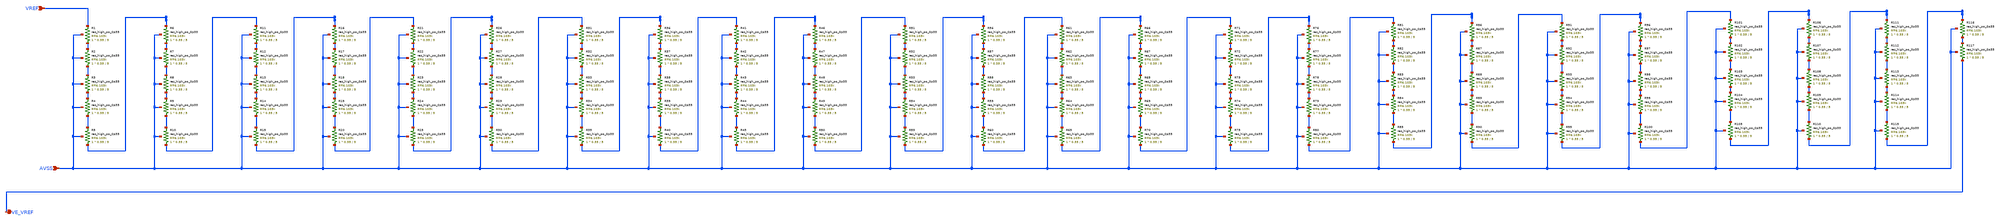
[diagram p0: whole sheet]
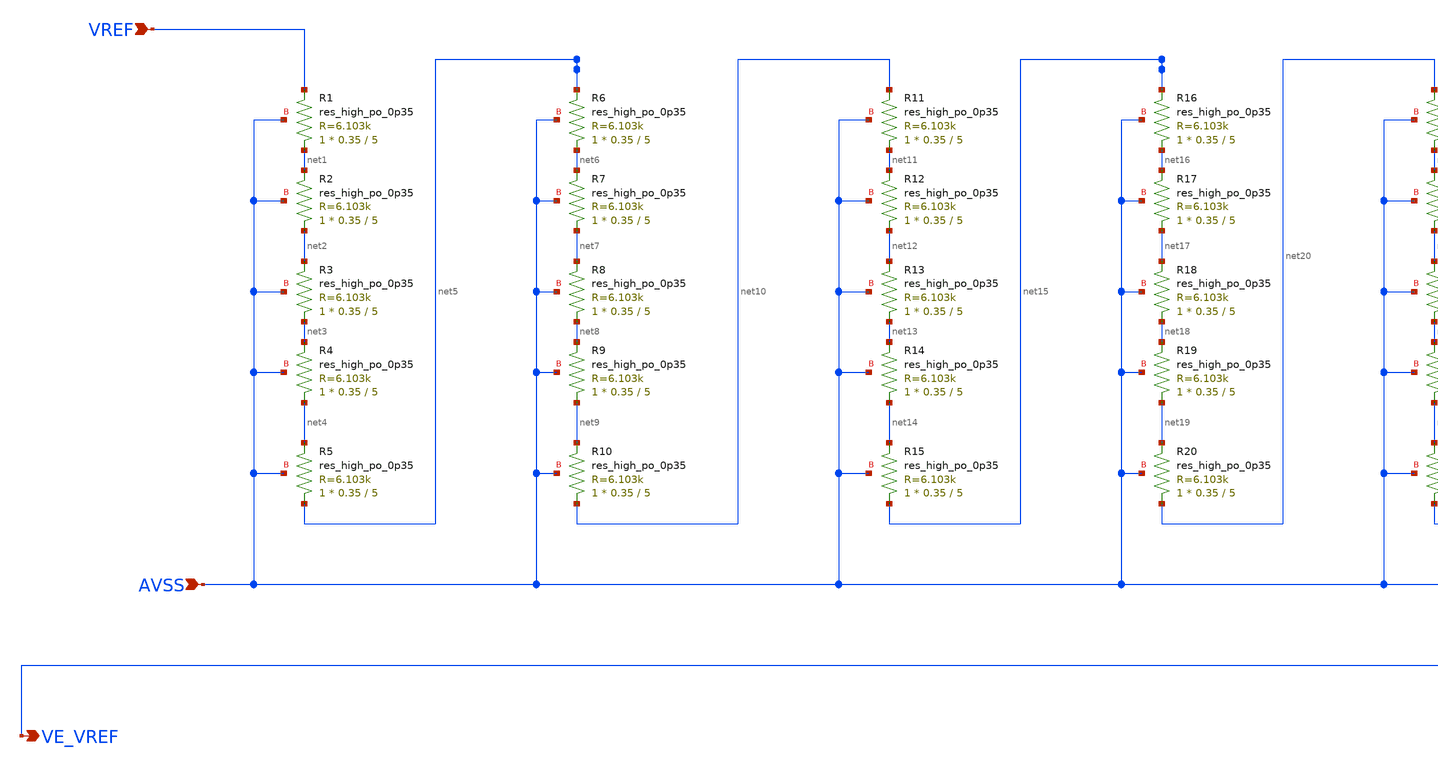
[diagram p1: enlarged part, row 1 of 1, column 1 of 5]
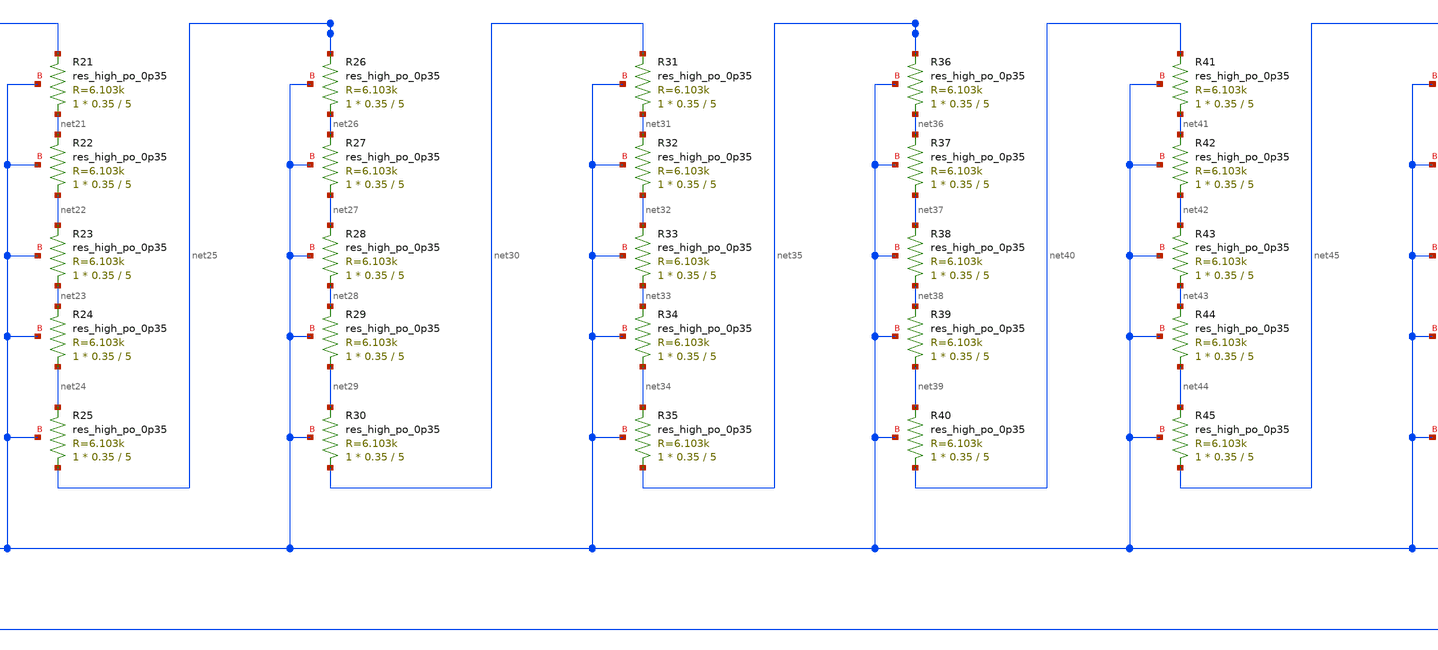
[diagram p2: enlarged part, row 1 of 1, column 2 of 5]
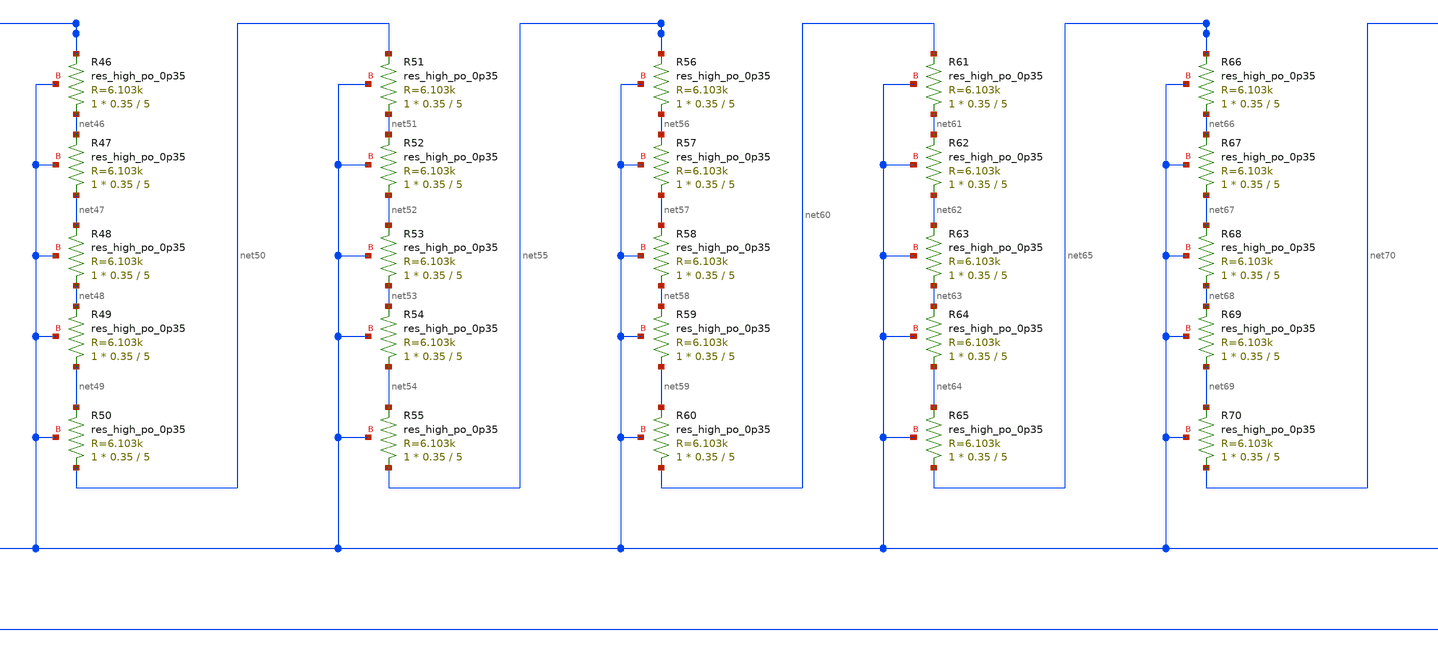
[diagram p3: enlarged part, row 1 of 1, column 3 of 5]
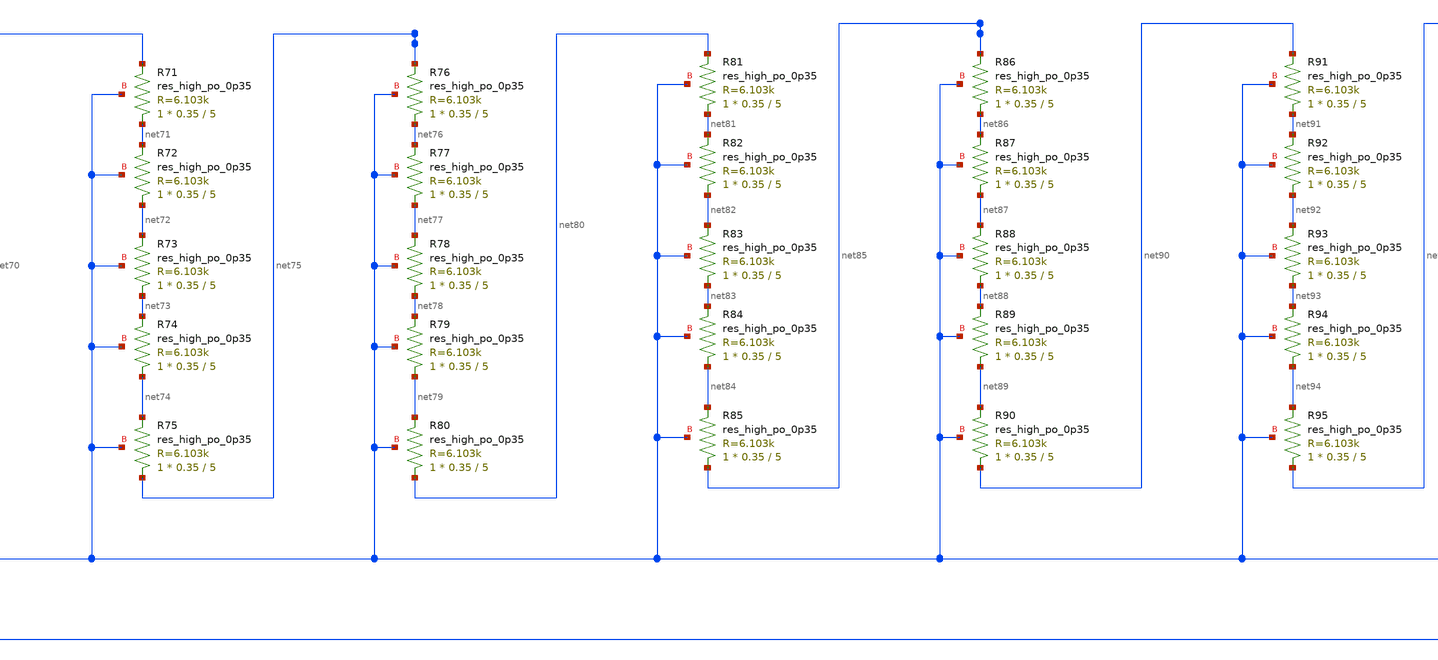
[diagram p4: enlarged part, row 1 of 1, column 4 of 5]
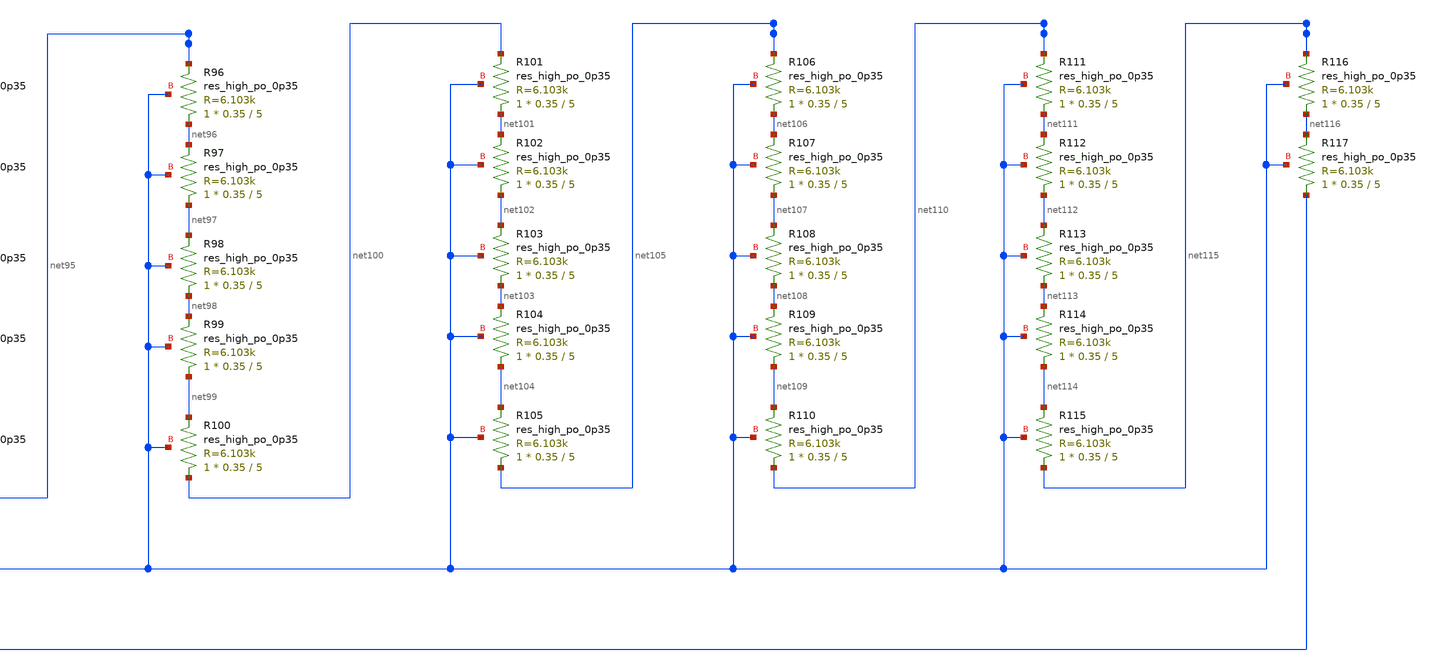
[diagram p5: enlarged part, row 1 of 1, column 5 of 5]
** sch_path: lef/bg2_res_array_vref.sch
**.subckt bg2_res_array_vref VREF VE_VREF AVSS
*.ipin VREF
*.opin VE_VREF
*.ipin AVSS
XR1 net1 VREF AVSS sky130_fd_pr__res_high_po_0p35 L=5 mult=1 m=1
XR2 net2 net1 AVSS sky130_fd_pr__res_high_po_0p35 L=5 mult=1 m=1
XR3 net3 net2 AVSS sky130_fd_pr__res_high_po_0p35 L=5 mult=1 m=1
XR4 net4 net3 AVSS sky130_fd_pr__res_high_po_0p35 L=5 mult=1 m=1
XR5 net5 net4 AVSS sky130_fd_pr__res_high_po_0p35 L=5 mult=1 m=1
XR6 net6 net5 AVSS sky130_fd_pr__res_high_po_0p35 L=5 mult=1 m=1
XR7 net7 net6 AVSS sky130_fd_pr__res_high_po_0p35 L=5 mult=1 m=1
XR8 net8 net7 AVSS sky130_fd_pr__res_high_po_0p35 L=5 mult=1 m=1
XR9 net9 net8 AVSS sky130_fd_pr__res_high_po_0p35 L=5 mult=1 m=1
XR10 net10 net9 AVSS sky130_fd_pr__res_high_po_0p35 L=5 mult=1 m=1
XR11 net11 net10 AVSS sky130_fd_pr__res_high_po_0p35 L=5 mult=1 m=1
XR12 net12 net11 AVSS sky130_fd_pr__res_high_po_0p35 L=5 mult=1 m=1
XR13 net13 net12 AVSS sky130_fd_pr__res_high_po_0p35 L=5 mult=1 m=1
XR14 net14 net13 AVSS sky130_fd_pr__res_high_po_0p35 L=5 mult=1 m=1
XR15 net15 net14 AVSS sky130_fd_pr__res_high_po_0p35 L=5 mult=1 m=1
XR16 net16 net15 AVSS sky130_fd_pr__res_high_po_0p35 L=5 mult=1 m=1
XR17 net17 net16 AVSS sky130_fd_pr__res_high_po_0p35 L=5 mult=1 m=1
XR18 net18 net17 AVSS sky130_fd_pr__res_high_po_0p35 L=5 mult=1 m=1
XR19 net19 net18 AVSS sky130_fd_pr__res_high_po_0p35 L=5 mult=1 m=1
XR20 net20 net19 AVSS sky130_fd_pr__res_high_po_0p35 L=5 mult=1 m=1
XR21 net21 net20 AVSS sky130_fd_pr__res_high_po_0p35 L=5 mult=1 m=1
XR22 net22 net21 AVSS sky130_fd_pr__res_high_po_0p35 L=5 mult=1 m=1
XR23 net23 net22 AVSS sky130_fd_pr__res_high_po_0p35 L=5 mult=1 m=1
XR24 net24 net23 AVSS sky130_fd_pr__res_high_po_0p35 L=5 mult=1 m=1
XR25 net25 net24 AVSS sky130_fd_pr__res_high_po_0p35 L=5 mult=1 m=1
XR26 net26 net25 AVSS sky130_fd_pr__res_high_po_0p35 L=5 mult=1 m=1
XR27 net27 net26 AVSS sky130_fd_pr__res_high_po_0p35 L=5 mult=1 m=1
XR28 net28 net27 AVSS sky130_fd_pr__res_high_po_0p35 L=5 mult=1 m=1
XR29 net29 net28 AVSS sky130_fd_pr__res_high_po_0p35 L=5 mult=1 m=1
XR30 net30 net29 AVSS sky130_fd_pr__res_high_po_0p35 L=5 mult=1 m=1
XR31 net31 net30 AVSS sky130_fd_pr__res_high_po_0p35 L=5 mult=1 m=1
XR32 net32 net31 AVSS sky130_fd_pr__res_high_po_0p35 L=5 mult=1 m=1
XR33 net33 net32 AVSS sky130_fd_pr__res_high_po_0p35 L=5 mult=1 m=1
XR34 net34 net33 AVSS sky130_fd_pr__res_high_po_0p35 L=5 mult=1 m=1
XR35 net35 net34 AVSS sky130_fd_pr__res_high_po_0p35 L=5 mult=1 m=1
XR36 net36 net35 AVSS sky130_fd_pr__res_high_po_0p35 L=5 mult=1 m=1
XR37 net37 net36 AVSS sky130_fd_pr__res_high_po_0p35 L=5 mult=1 m=1
XR38 net38 net37 AVSS sky130_fd_pr__res_high_po_0p35 L=5 mult=1 m=1
XR39 net39 net38 AVSS sky130_fd_pr__res_high_po_0p35 L=5 mult=1 m=1
XR40 net40 net39 AVSS sky130_fd_pr__res_high_po_0p35 L=5 mult=1 m=1
XR41 net41 net40 AVSS sky130_fd_pr__res_high_po_0p35 L=5 mult=1 m=1
XR42 net42 net41 AVSS sky130_fd_pr__res_high_po_0p35 L=5 mult=1 m=1
XR43 net43 net42 AVSS sky130_fd_pr__res_high_po_0p35 L=5 mult=1 m=1
XR44 net44 net43 AVSS sky130_fd_pr__res_high_po_0p35 L=5 mult=1 m=1
XR45 net45 net44 AVSS sky130_fd_pr__res_high_po_0p35 L=5 mult=1 m=1
XR46 net46 net45 AVSS sky130_fd_pr__res_high_po_0p35 L=5 mult=1 m=1
XR47 net47 net46 AVSS sky130_fd_pr__res_high_po_0p35 L=5 mult=1 m=1
XR48 net48 net47 AVSS sky130_fd_pr__res_high_po_0p35 L=5 mult=1 m=1
XR49 net49 net48 AVSS sky130_fd_pr__res_high_po_0p35 L=5 mult=1 m=1
XR50 net50 net49 AVSS sky130_fd_pr__res_high_po_0p35 L=5 mult=1 m=1
XR51 net51 net50 AVSS sky130_fd_pr__res_high_po_0p35 L=5 mult=1 m=1
XR52 net52 net51 AVSS sky130_fd_pr__res_high_po_0p35 L=5 mult=1 m=1
XR53 net53 net52 AVSS sky130_fd_pr__res_high_po_0p35 L=5 mult=1 m=1
XR54 net54 net53 AVSS sky130_fd_pr__res_high_po_0p35 L=5 mult=1 m=1
XR55 net55 net54 AVSS sky130_fd_pr__res_high_po_0p35 L=5 mult=1 m=1
XR56 net56 net55 AVSS sky130_fd_pr__res_high_po_0p35 L=5 mult=1 m=1
XR57 net57 net56 AVSS sky130_fd_pr__res_high_po_0p35 L=5 mult=1 m=1
XR58 net58 net57 AVSS sky130_fd_pr__res_high_po_0p35 L=5 mult=1 m=1
XR59 net59 net58 AVSS sky130_fd_pr__res_high_po_0p35 L=5 mult=1 m=1
XR60 net60 net59 AVSS sky130_fd_pr__res_high_po_0p35 L=5 mult=1 m=1
XR61 net61 net60 AVSS sky130_fd_pr__res_high_po_0p35 L=5 mult=1 m=1
XR62 net62 net61 AVSS sky130_fd_pr__res_high_po_0p35 L=5 mult=1 m=1
XR63 net63 net62 AVSS sky130_fd_pr__res_high_po_0p35 L=5 mult=1 m=1
XR64 net64 net63 AVSS sky130_fd_pr__res_high_po_0p35 L=5 mult=1 m=1
XR65 net65 net64 AVSS sky130_fd_pr__res_high_po_0p35 L=5 mult=1 m=1
XR66 net66 net65 AVSS sky130_fd_pr__res_high_po_0p35 L=5 mult=1 m=1
XR67 net67 net66 AVSS sky130_fd_pr__res_high_po_0p35 L=5 mult=1 m=1
XR68 net68 net67 AVSS sky130_fd_pr__res_high_po_0p35 L=5 mult=1 m=1
XR69 net69 net68 AVSS sky130_fd_pr__res_high_po_0p35 L=5 mult=1 m=1
XR70 net70 net69 AVSS sky130_fd_pr__res_high_po_0p35 L=5 mult=1 m=1
XR71 net71 net70 AVSS sky130_fd_pr__res_high_po_0p35 L=5 mult=1 m=1
XR72 net72 net71 AVSS sky130_fd_pr__res_high_po_0p35 L=5 mult=1 m=1
XR73 net73 net72 AVSS sky130_fd_pr__res_high_po_0p35 L=5 mult=1 m=1
XR74 net74 net73 AVSS sky130_fd_pr__res_high_po_0p35 L=5 mult=1 m=1
XR75 net75 net74 AVSS sky130_fd_pr__res_high_po_0p35 L=5 mult=1 m=1
XR76 net76 net75 AVSS sky130_fd_pr__res_high_po_0p35 L=5 mult=1 m=1
XR77 net77 net76 AVSS sky130_fd_pr__res_high_po_0p35 L=5 mult=1 m=1
XR78 net78 net77 AVSS sky130_fd_pr__res_high_po_0p35 L=5 mult=1 m=1
XR79 net79 net78 AVSS sky130_fd_pr__res_high_po_0p35 L=5 mult=1 m=1
XR80 net80 net79 AVSS sky130_fd_pr__res_high_po_0p35 L=5 mult=1 m=1
XR81 net81 net80 AVSS sky130_fd_pr__res_high_po_0p35 L=5 mult=1 m=1
XR82 net82 net81 AVSS sky130_fd_pr__res_high_po_0p35 L=5 mult=1 m=1
XR83 net83 net82 AVSS sky130_fd_pr__res_high_po_0p35 L=5 mult=1 m=1
XR84 net84 net83 AVSS sky130_fd_pr__res_high_po_0p35 L=5 mult=1 m=1
XR85 net85 net84 AVSS sky130_fd_pr__res_high_po_0p35 L=5 mult=1 m=1
XR86 net86 net85 AVSS sky130_fd_pr__res_high_po_0p35 L=5 mult=1 m=1
XR87 net87 net86 AVSS sky130_fd_pr__res_high_po_0p35 L=5 mult=1 m=1
XR88 net88 net87 AVSS sky130_fd_pr__res_high_po_0p35 L=5 mult=1 m=1
XR89 net89 net88 AVSS sky130_fd_pr__res_high_po_0p35 L=5 mult=1 m=1
XR90 net90 net89 AVSS sky130_fd_pr__res_high_po_0p35 L=5 mult=1 m=1
XR91 net91 net90 AVSS sky130_fd_pr__res_high_po_0p35 L=5 mult=1 m=1
XR92 net92 net91 AVSS sky130_fd_pr__res_high_po_0p35 L=5 mult=1 m=1
XR93 net93 net92 AVSS sky130_fd_pr__res_high_po_0p35 L=5 mult=1 m=1
XR94 net94 net93 AVSS sky130_fd_pr__res_high_po_0p35 L=5 mult=1 m=1
XR95 net95 net94 AVSS sky130_fd_pr__res_high_po_0p35 L=5 mult=1 m=1
XR96 net96 net95 AVSS sky130_fd_pr__res_high_po_0p35 L=5 mult=1 m=1
XR97 net97 net96 AVSS sky130_fd_pr__res_high_po_0p35 L=5 mult=1 m=1
XR98 net98 net97 AVSS sky130_fd_pr__res_high_po_0p35 L=5 mult=1 m=1
XR99 net99 net98 AVSS sky130_fd_pr__res_high_po_0p35 L=5 mult=1 m=1
XR100 net100 net99 AVSS sky130_fd_pr__res_high_po_0p35 L=5 mult=1 m=1
XR101 net101 net100 AVSS sky130_fd_pr__res_high_po_0p35 L=5 mult=1 m=1
XR102 net102 net101 AVSS sky130_fd_pr__res_high_po_0p35 L=5 mult=1 m=1
XR103 net103 net102 AVSS sky130_fd_pr__res_high_po_0p35 L=5 mult=1 m=1
XR104 net104 net103 AVSS sky130_fd_pr__res_high_po_0p35 L=5 mult=1 m=1
XR105 net105 net104 AVSS sky130_fd_pr__res_high_po_0p35 L=5 mult=1 m=1
XR106 net106 net105 AVSS sky130_fd_pr__res_high_po_0p35 L=5 mult=1 m=1
XR107 net107 net106 AVSS sky130_fd_pr__res_high_po_0p35 L=5 mult=1 m=1
XR108 net108 net107 AVSS sky130_fd_pr__res_high_po_0p35 L=5 mult=1 m=1
XR109 net109 net108 AVSS sky130_fd_pr__res_high_po_0p35 L=5 mult=1 m=1
XR110 net110 net109 AVSS sky130_fd_pr__res_high_po_0p35 L=5 mult=1 m=1
XR111 net111 net110 AVSS sky130_fd_pr__res_high_po_0p35 L=5 mult=1 m=1
XR112 net112 net111 AVSS sky130_fd_pr__res_high_po_0p35 L=5 mult=1 m=1
XR113 net113 net112 AVSS sky130_fd_pr__res_high_po_0p35 L=5 mult=1 m=1
XR114 net114 net113 AVSS sky130_fd_pr__res_high_po_0p35 L=5 mult=1 m=1
XR115 net115 net114 AVSS sky130_fd_pr__res_high_po_0p35 L=5 mult=1 m=1
XR116 net116 net115 AVSS sky130_fd_pr__res_high_po_0p35 L=5 mult=1 m=1
XR117 VE_VREF net116 AVSS sky130_fd_pr__res_high_po_0p35 L=5 mult=1 m=1
**.ends
.end
